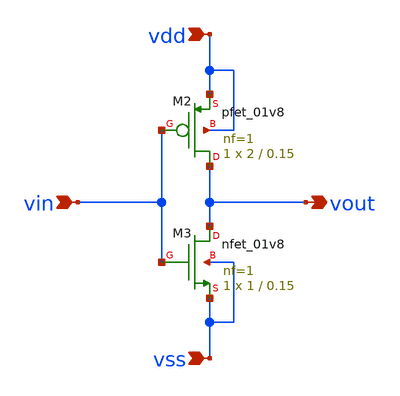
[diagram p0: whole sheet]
** sch_path: VLSI/P_D_S_TEST_05/VLSI_TEST_05 (Post_Design_Simulation))/inv_vtc_2.1.sch
**.subckt inv_vtc_2.1 vin vout vdd vss
*.ipin vin
*.opin vout
*.ipin vdd
*.ipin vss
XM2 vout vin vdd vdd sky130_fd_pr__pfet_01v8 L=0.15 W=2 nf=1 ad='int((nf+1)/2) * W/nf * 0.29' as='int((nf+2)/2) * W/nf * 0.29'
+ pd='2*int((nf+1)/2) * (W/nf + 0.29)' ps='2*int((nf+2)/2) * (W/nf + 0.29)' nrd='0.29 / W' nrs='0.29 / W'
+ sa=0 sb=0 sd=0 mult=1 m=1
XM3 vout vin vss vss sky130_fd_pr__nfet_01v8 L=0.15 W=1 nf=1 ad='int((nf+1)/2) * W/nf * 0.29' as='int((nf+2)/2) * W/nf * 0.29'
+ pd='2*int((nf+1)/2) * (W/nf + 0.29)' ps='2*int((nf+2)/2) * (W/nf + 0.29)' nrd='0.29 / W' nrs='0.29 / W'
+ sa=0 sb=0 sd=0 mult=1 m=1
**.ends
.end
